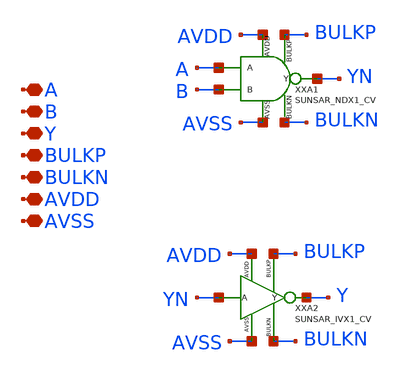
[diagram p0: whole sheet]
** sch_path: design/SUN_SAR9B_SKY130NM/SUNSAR_ANX1_CV.sch
**.subckt SUNSAR_ANX1_CV A B Y BULKP BULKN AVDD AVSS
*.iopin A
*.iopin B
*.iopin Y
*.iopin BULKP
*.iopin BULKN
*.iopin AVDD
*.iopin AVSS
XXA1 A B YN BULKP BULKN AVDD AVSS SUNSAR_NDX1_CV
XXA2 YN Y BULKP BULKN AVDD AVSS SUNSAR_IVX1_CV
**.ends
.end
